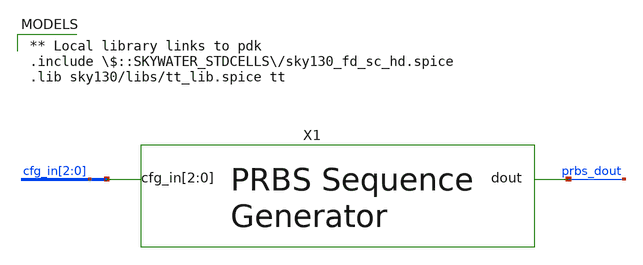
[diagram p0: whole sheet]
** sch_path: xschem/prb_gen_tb.sch
 ** Local library links to pdk
.include $::SKYWATER_STDCELLS/sky130_fd_sc_hd.spice
.lib sky130/libs/tt_lib.spice tt
**.subckt prb_gen_tb
X1 cfg_in[2] cfg_in[1] cfg_in[0] prbs_dout VDD GND prbs_gen
**.ends

* expanding   symbol:  xschem/prbs_gen.sym # of pins=2
** sym_path: xschem/prbs_gen.sym
** sch_path: xschem/prbs_gen.sch
.subckt prbs_gen cfg_in[2] cfg_in[1] cfg_in[0] dout VDD GND
*.opin dout
*.ipin cfg_in[2],cfg_in[1],cfg_in[0]
x8 net12 net5 GND GND VDD VDD net17 net5 sky130_fd_sc_hd__dfxbp_1
x16 net1 GND GND VDD VDD net13 sky130_fd_sc_hd__clkbuf_1
x5 net2 GND GND VDD VDD net3 sky130_fd_sc_hd__clkinv_1
x6 net3 GND GND VDD VDD net4 sky130_fd_sc_hd__clkinv_1
x7 net4 GND GND VDD VDD net1 sky130_fd_sc_hd__clkinv_1
x15 net13 GND GND VDD VDD net14 sky130_fd_sc_hd__clkbuf_1
x9 net5 net6 GND GND VDD VDD net18 net6 sky130_fd_sc_hd__dfxbp_1
x10 net6 net7 GND GND VDD VDD net19 net7 sky130_fd_sc_hd__dfxbp_1
x11 net7 net8 GND GND VDD VDD net20 net8 sky130_fd_sc_hd__dfxbp_1
x12 net8 net9 GND GND VDD VDD net21 net9 sky130_fd_sc_hd__dfxbp_1
x13 net9 net10 GND GND VDD VDD net22 net10 sky130_fd_sc_hd__dfxbp_1
x14 net10 net11 GND GND VDD VDD net23 net11 sky130_fd_sc_hd__dfxbp_1
x1 net14 GND GND VDD VDD net15 sky130_fd_sc_hd__clkbuf_1
x2 net15 GND GND VDD VDD net12 sky130_fd_sc_hd__clkbuf_1
x3 net16 GND GND VDD VDD net2 sky130_fd_sc_hd__clkinv_1
x4 net1 GND GND VDD VDD net16 sky130_fd_sc_hd__clkinv_1
x17 clk_0 clken_0 GND GND VDD VDD dout sky130_fd_sc_hd__einvn_1
x19 cfg_in[2] cfg_in[1] cfg_in[0] GND GND VDD VDD clken_0 sky130_fd_sc_hd__or3_1
x25 cfg_in[2] cfg_in[1] cfg_in[0] GND GND VDD VDD clken_1 sky130_fd_sc_hd__or3b_1
x26 net12 GND GND VDD VDD clk_0 sky130_fd_sc_hd__clkbuf_1
x28 net5 GND GND VDD VDD clk_1 sky130_fd_sc_hd__clkbuf_1
x29 net6 GND GND VDD VDD clk_2 sky130_fd_sc_hd__clkbuf_1
x30 net7 GND GND VDD VDD clk_3 sky130_fd_sc_hd__clkbuf_1
x31 net8 GND GND VDD VDD clk_4 sky130_fd_sc_hd__clkbuf_1
x32 net9 GND GND VDD VDD clk_5 sky130_fd_sc_hd__clkbuf_1
x33 net10 GND GND VDD VDD clk_6 sky130_fd_sc_hd__clkbuf_1
x34 net11 GND GND VDD VDD clk_7 sky130_fd_sc_hd__clkbuf_1
x20 cfg_in[2] cfg_in[0] cfg_in[1] GND GND VDD VDD clken_2 sky130_fd_sc_hd__or3b_1
x21 cfg_in[2] cfg_in[1] cfg_in[0] GND GND VDD VDD clken_3 sky130_fd_sc_hd__nand3b_1
x22 cfg_in[0] cfg_in[1] cfg_in[2] GND GND VDD VDD clken_4 sky130_fd_sc_hd__or3b_1
x23 cfg_in[1] cfg_in[0] cfg_in[2] GND GND VDD VDD clken_5 sky130_fd_sc_hd__nand3b_1
x35 cfg_in[0] cfg_in[2] cfg_in[1] GND GND VDD VDD clken_6 sky130_fd_sc_hd__nand3b_1
x36 cfg_in[2] cfg_in[1] cfg_in[0] GND GND VDD VDD clken_7 sky130_fd_sc_hd__nand3_1
x18 clk_1 clken_1 GND GND VDD VDD dout sky130_fd_sc_hd__einvn_1
x24 clk_2 clken_2 GND GND VDD VDD dout sky130_fd_sc_hd__einvn_1
x27 clk_3 clken_3 GND GND VDD VDD dout sky130_fd_sc_hd__einvn_1
x37 clk_4 clken_4 GND GND VDD VDD dout sky130_fd_sc_hd__einvn_1
x38 clk_5 clken_5 GND GND VDD VDD dout sky130_fd_sc_hd__einvn_1
x39 clk_6 clken_6 GND GND VDD VDD dout sky130_fd_sc_hd__einvn_1
x40 clk_7 clken_7 GND GND VDD VDD dout sky130_fd_sc_hd__einvn_1
.ends

**** begin user architecture code


* power voltage
vvdd VDD 0 1.5

** STATIC CONTOL


** Signal
vcfg2 cfg_in[2]  0  0
vcfg1 cfg_in[1]  0  0
vcfg0 cfg_in[0]  0  0




.control
save all
set temp=27

* RUN SIMULATION
tran 1p 12n

* OUTPUT
set hcopydevtype = svg
hardcopy ./prbs_tb.svg x1.clk_0 prbs_dout title 'PRBS Output'
hardcopy ./prbs_clks.svg x1.clken_0 x1.clken_1+2 x1.clken_2+4 x1.clken_3+6 x1.clken_4+8 x1.clken_5+10
+ x1.clken_6+12 x1.clken_7+14 title 'prbs clkens'

.endc


**** end user architecture code
.end
